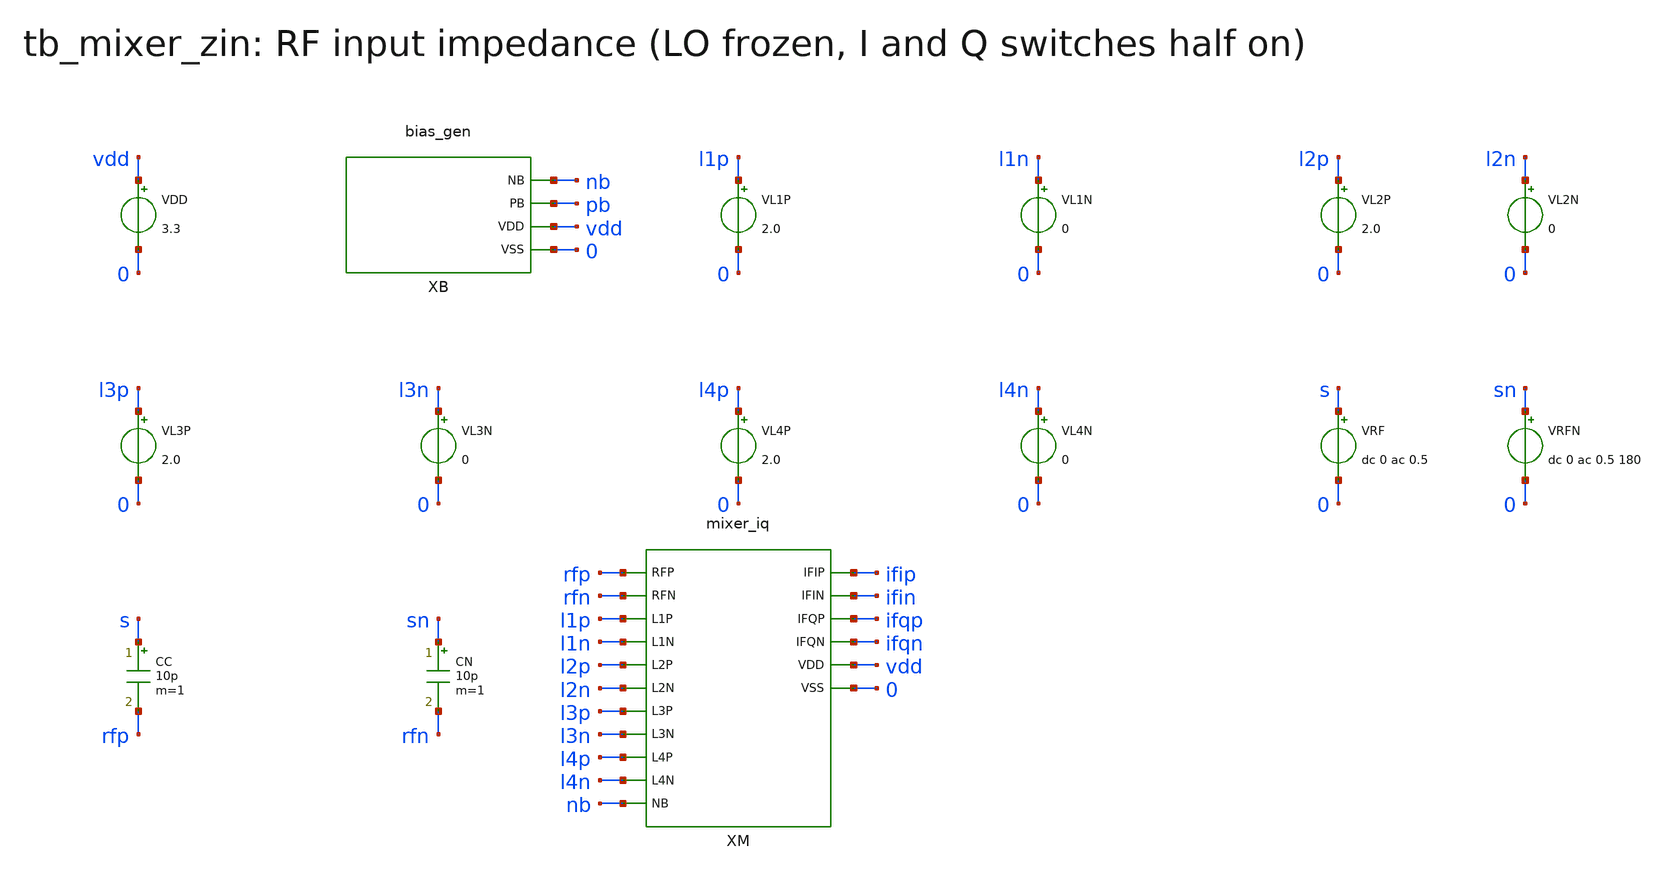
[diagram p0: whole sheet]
** sch_path: v1_claude/xschem/tb_mixer_zin.sch
**.subckt tb_mixer_zin
VDD vdd 0 3.3
XB nb pb vdd 0 bias_gen
VL1P l1p 0 2.0
VL1N l1n 0 0
VL2P l2p 0 2.0
VL2N l2n 0 0
VL3P l3p 0 2.0
VL3N l3n 0 0
VL4P l4p 0 2.0
VL4N l4n 0 0
VRF s 0 dc 0 ac 0.5
VRFN sn 0 dc 0 ac 0.5 180
CC s rfp 10p m=1
CN sn rfn 10p m=1
XM rfp rfn l1p l1n l2p l2n l3p l3n l4p l4n nb ifip ifin ifqp ifqn vdd 0 mixer_iq
**** begin user architecture code
 .include $::180MCU_MODELS/design.ngspice
.lib $::180MCU_MODELS/sm141064.ngspice typical
.lib $::180MCU_MODELS/sm141064.ngspice res_typical
.lib $::180MCU_MODELS/sm141064.ngspice mimcap_typical

.control
set num_threads=1
op
echo RES itail=$&@m.xm.xmti.m0[id] vgm=$&v(xm.tI) vop=$&v(ifip) vbrf=$&v(rfp)
ac lin 3 1.55e9 1.6e9
let zin = (v(rfp)-v(rfn))/(-i(VRF))
let s11 = (zin-100)/(zin+100)
print real(zin) imag(zin) db(s11)
.endc

**** end user architecture code
**.ends
.end
